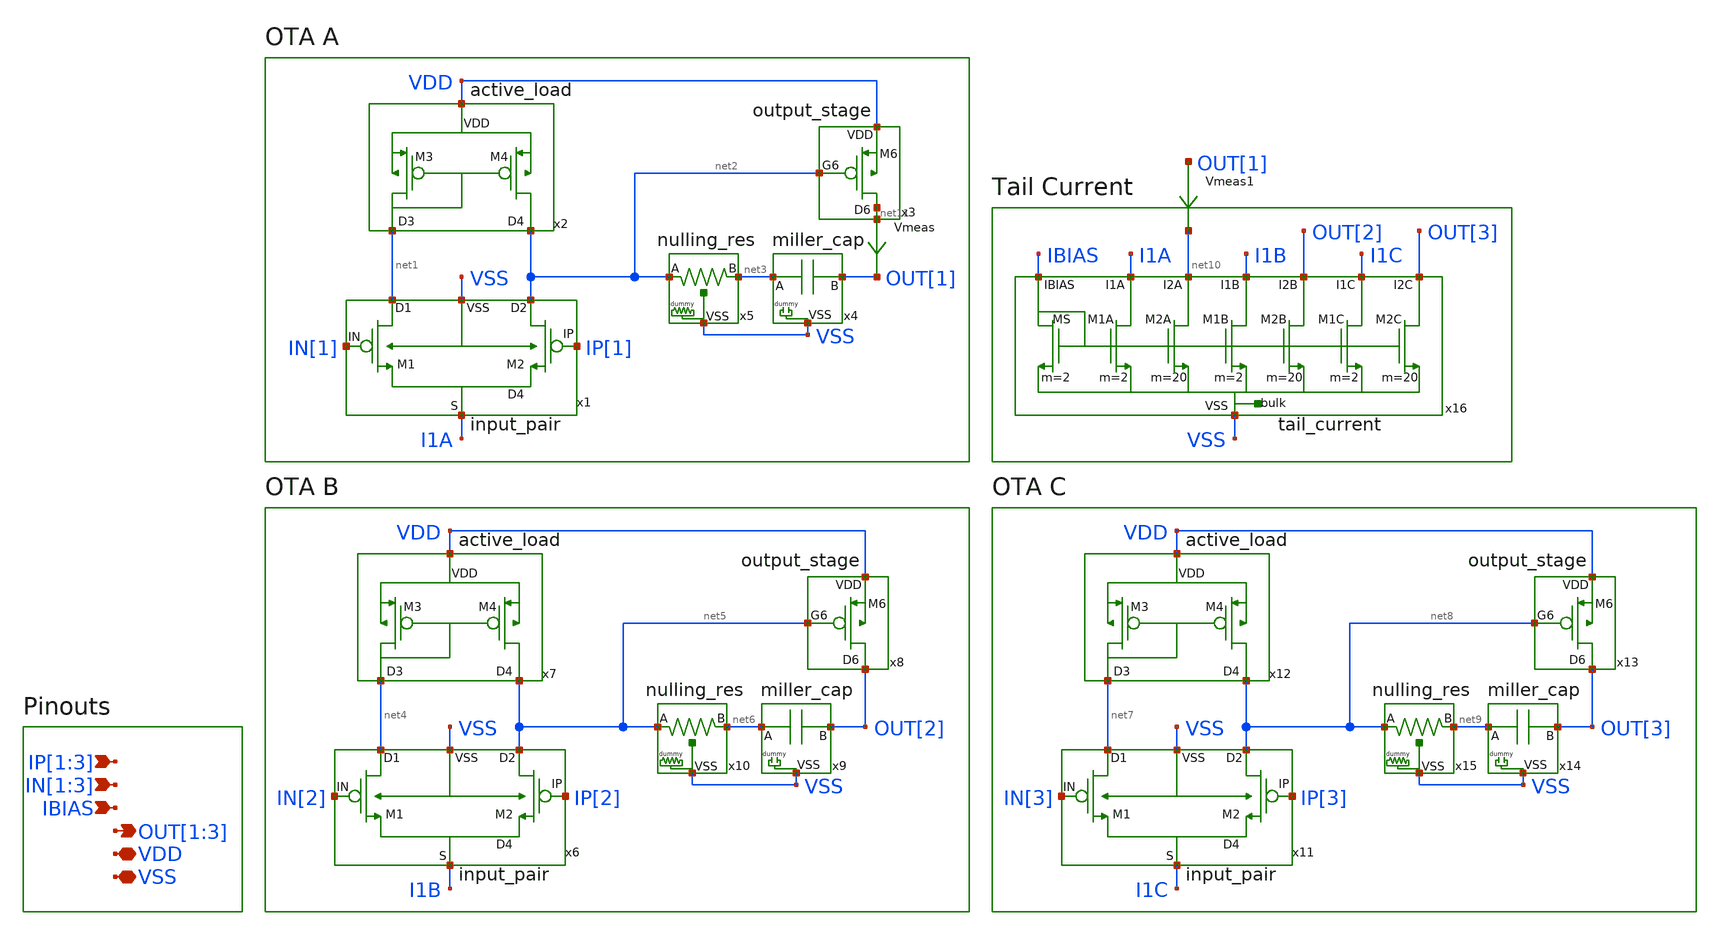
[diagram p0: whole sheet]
** sch_path: designs/libs/core_ota/three_single_ended_ota/three_single_ended_ota.sch
**.subckt three_single_ended_ota IP[1],IP[2],IP[3] IN[1],IN[2],IN[3] VDD VSS IBIAS
*+ OUT[1],OUT[2],OUT[3]
*.ipin IP[1],IP[2],IP[3]
*.ipin IN[1],IN[2],IN[3]
*.iopin VDD
*.iopin VSS
*.ipin IBIAS
*.opin OUT[1],OUT[2],OUT[3]
x1 IN[1] IP[1] I1A net2 net1 VSS input_pair
x3 net11 VDD net2 output_stage
x4 net3 OUT[1] VSS miller_cap
x5 net2 net3 VSS nulling_res
x6 IN[2] IP[2] I1B net5 net4 VSS input_pair
x11 IN[3] IP[3] I1C net8 net7 VSS input_pair
x8 OUT[2] VDD net5 output_stage
x13 OUT[3] VDD net8 output_stage
x9 net6 OUT[2] VSS miller_cap
x14 net9 OUT[3] VSS miller_cap
x10 net5 net6 VSS nulling_res
x15 net8 net9 VSS nulling_res
x2 net1 net2 VDD active_load
x7 net4 net5 VDD active_load
x12 net7 net8 VDD active_load
x16 IBIAS I1A net10 I1B OUT[2] I1C OUT[3] VSS tail_current
Vmeas net11 OUT[1] 0
.save i(vmeas)
Vmeas1 OUT[1] net10 0
.save i(vmeas1)
**.ends
.end
